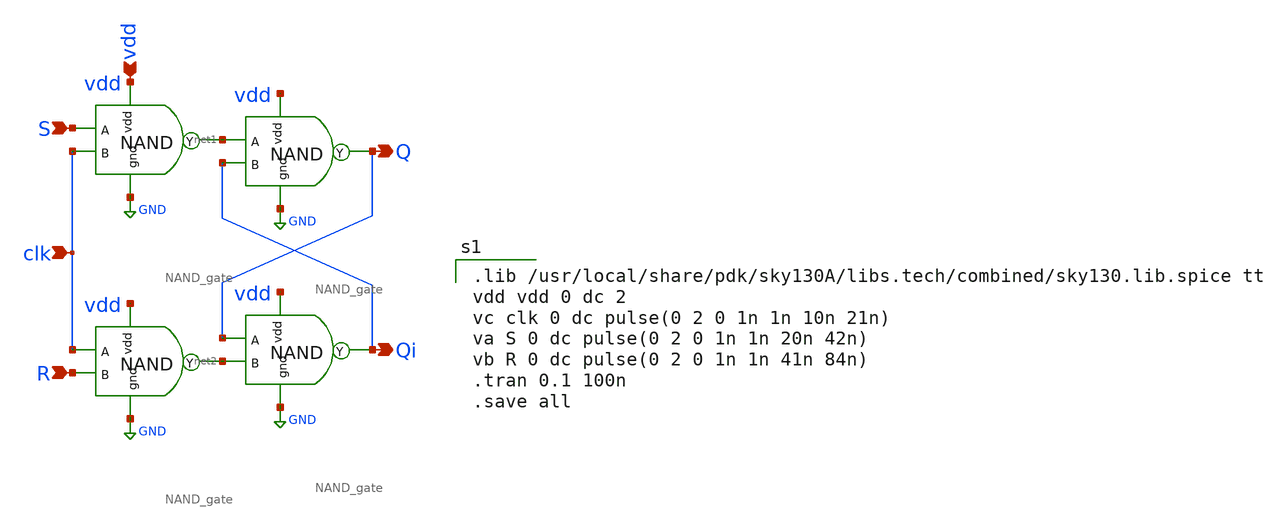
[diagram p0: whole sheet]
** sch_path: Circuit Files/circuits/circuits/SR_ff.sch
**.subckt SR_ff clk S R vdd Q Qi
*.ipin clk
*.ipin S
*.ipin R
*.ipin vdd
*.opin Q
*.opin Qi
x1 vdd net1 S clk GND NAND_gate
x3 vdd Q net1 Qi GND NAND_gate
x4 vdd net2 clk R GND NAND_gate
x5 vdd Qi Q net2 GND NAND_gate
**** begin user architecture code

.lib /usr/local/share/pdk/sky130A/libs.tech/combined/sky130.lib.spice tt
vdd vdd 0 dc 2
vc clk 0 dc pulse(0 2 0 1n 1n 10n 21n)
va S 0 dc pulse(0 2 0 1n 1n 20n 42n)
vb R 0 dc pulse(0 2 0 1n 1n 41n 84n)
.tran 0.1 100n
.save all

**** end user architecture code
**.ends

* expanding   symbol:  daVLSI_World/gates/NAND_gate.sym # of pins=5
** sym_path: Circuit Files/Logic gate design using MOSFETS/gates/NAND_gate.sym
** sch_path: Circuit Files/Logic gate design using MOSFETS/gates/NAND_gate.sch
.subckt NAND_gate vdd Y A B gnd
*.ipin A
*.ipin B
*.opin Y
*.ipin vdd
*.ipin gnd
XM1 Y A net1 gnd sky130_fd_pr__nfet_01v8 L=0.15 W=1 nf=1 ad='int((nf+1)/2) * W/nf * 0.29' as='int((nf+2)/2) * W/nf * 0.29'
+ pd='2*int((nf+1)/2) * (W/nf + 0.29)' ps='2*int((nf+2)/2) * (W/nf + 0.29)' nrd='0.29 / W' nrs='0.29 / W'
+ sa=0 sb=0 sd=0 mult=1 m=1
XM2 net1 B gnd gnd sky130_fd_pr__nfet_01v8 L=0.15 W=1 nf=1 ad='int((nf+1)/2) * W/nf * 0.29' as='int((nf+2)/2) * W/nf * 0.29'
+ pd='2*int((nf+1)/2) * (W/nf + 0.29)' ps='2*int((nf+2)/2) * (W/nf + 0.29)' nrd='0.29 / W' nrs='0.29 / W'
+ sa=0 sb=0 sd=0 mult=1 m=1
XM3 Y A vdd vdd sky130_fd_pr__pfet_01v8 L=0.15 W=2 nf=1 ad='int((nf+1)/2) * W/nf * 0.29' as='int((nf+2)/2) * W/nf * 0.29'
+ pd='2*int((nf+1)/2) * (W/nf + 0.29)' ps='2*int((nf+2)/2) * (W/nf + 0.29)' nrd='0.29 / W' nrs='0.29 / W'
+ sa=0 sb=0 sd=0 mult=1 m=1
XM4 Y B vdd vdd sky130_fd_pr__pfet_01v8 L=0.15 W=2 nf=1 ad='int((nf+1)/2) * W/nf * 0.29' as='int((nf+2)/2) * W/nf * 0.29'
+ pd='2*int((nf+1)/2) * (W/nf + 0.29)' ps='2*int((nf+2)/2) * (W/nf + 0.29)' nrd='0.29 / W' nrs='0.29 / W'
+ sa=0 sb=0 sd=0 mult=1 m=1
.ends

.GLOBAL GND
.end
